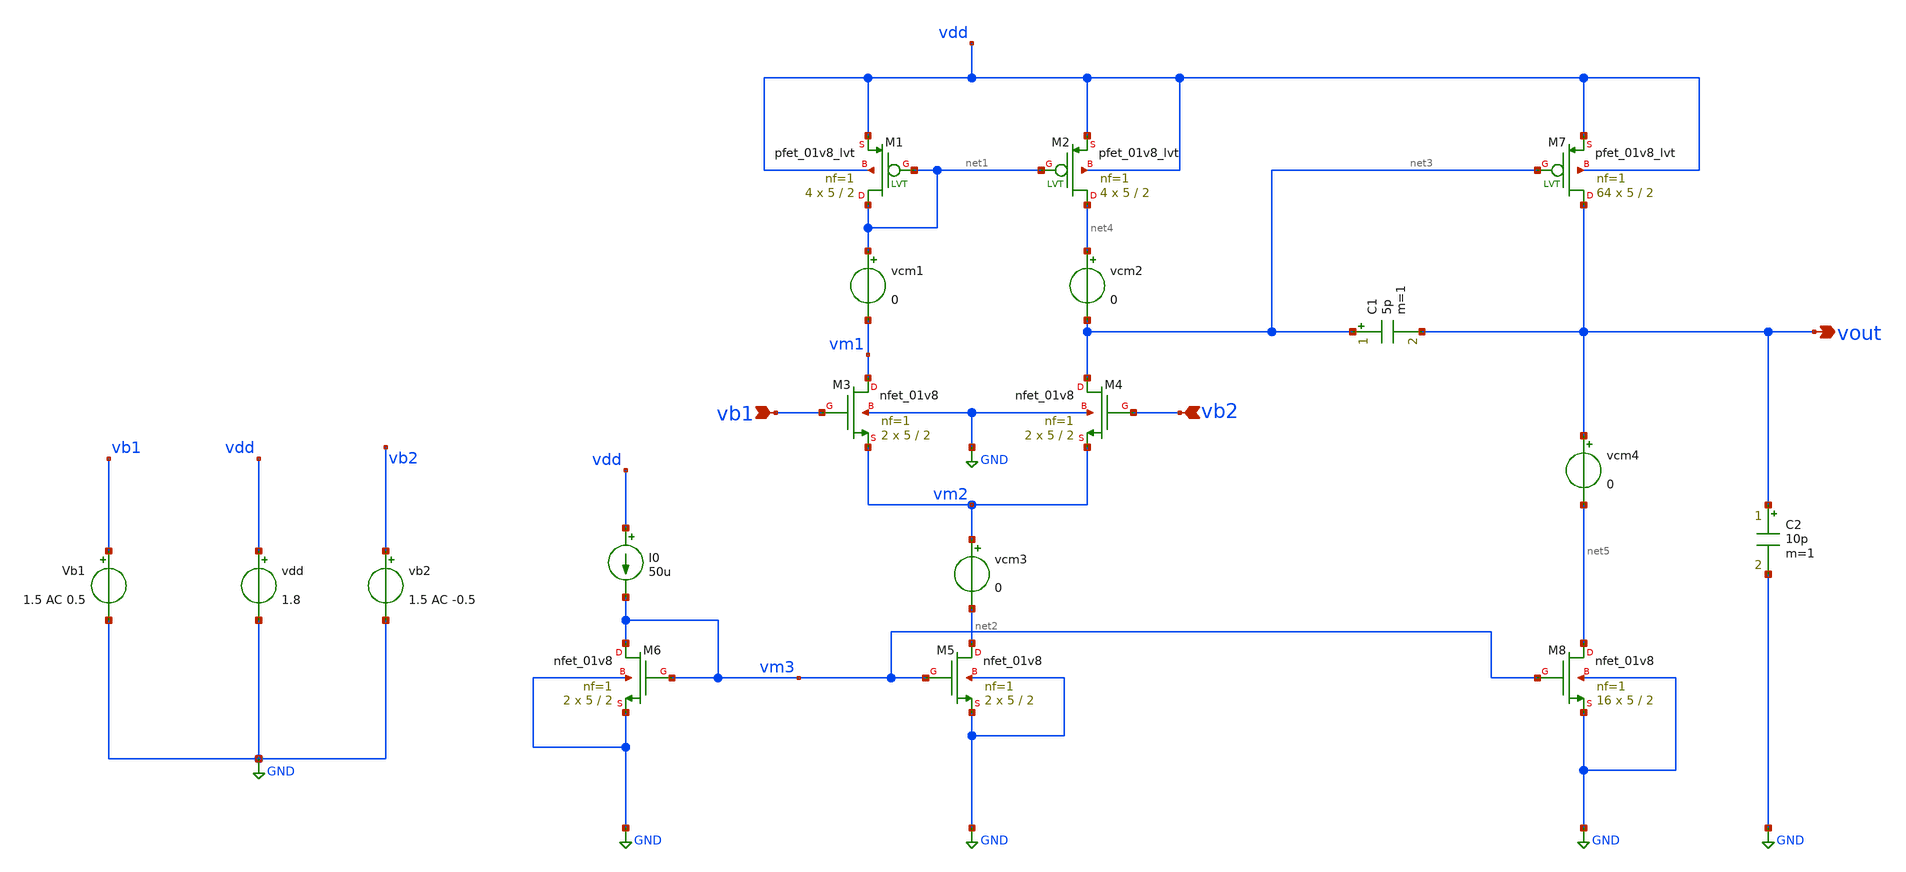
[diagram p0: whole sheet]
** sch_path: testbenches/Two_Stage_Differential_OpAmp_AC_Analysis.sch
**.subckt Two_Stage_Differential_OpAmp_AC_Analysis vb1 vout vb2
*.ipin vb1
*.opin vout
*.ipin vb2
XM5 net2 vm3 GND GND sky130_fd_pr__nfet_01v8 L=2 W=5 nf=1 ad='int((1 + 1)/2) * 5 / 1 * 0.29' as='int((1 + 2)/2) * 5 / 1 * 0.29'
+ pd='2*int((1 + 1)/2) * (5 / 1 + 0.29)' ps='2*int((1 + 2)/2) * (5 / 1 + 0.29)' nrd='0.29 / 5 ' nrs='0.29 / 5 '
+ sa=0 sb=0 sd=0 mult=2 m=2
I0 vdd vm3 50u
XM2 net4 net1 vdd vdd sky130_fd_pr__pfet_01v8_lvt L=2 W=5 nf=1 ad='int((1 + 1)/2) * 5 / 1 * 0.29' as='int((1 + 2)/2) * 5 / 1 * 0.29'
+ pd='2*int((1 + 1)/2) * (5 / 1 + 0.29)' ps='2*int((1 + 2)/2) * (5 / 1 + 0.29)' nrd='0.29 / 5 ' nrs='0.29 / 5 '
+ sa=0 sb=0 sd=0 mult=4 m=4
XM3 vm1 vb1 vm2 GND sky130_fd_pr__nfet_01v8 L=2 W=5 nf=1 ad='int((1 + 1)/2) * 5 / 1 * 0.29' as='int((1 + 2)/2) * 5 / 1 * 0.29'
+ pd='2*int((1 + 1)/2) * (5 / 1 + 0.29)' ps='2*int((1 + 2)/2) * (5 / 1 + 0.29)' nrd='0.29 / 5 ' nrs='0.29 / 5 '
+ sa=0 sb=0 sd=0 mult=2 m=2
XM4 net3 vb2 vm2 GND sky130_fd_pr__nfet_01v8 L=2 W=5 nf=1 ad='int((1 + 1)/2) * 5 / 1 * 0.29' as='int((1 + 2)/2) * 5 / 1 * 0.29'
+ pd='2*int((1 + 1)/2) * (5 / 1 + 0.29)' ps='2*int((1 + 2)/2) * (5 / 1 + 0.29)' nrd='0.29 / 5 ' nrs='0.29 / 5 '
+ sa=0 sb=0 sd=0 mult=2 m=2
XM6 vm3 vm3 GND GND sky130_fd_pr__nfet_01v8 L=2 W=5 nf=1 ad='int((1 + 1)/2) * 5 / 1 * 0.29' as='int((1 + 2)/2) * 5 / 1 * 0.29'
+ pd='2*int((1 + 1)/2) * (5 / 1 + 0.29)' ps='2*int((1 + 2)/2) * (5 / 1 + 0.29)' nrd='0.29 / 5 ' nrs='0.29 / 5 '
+ sa=0 sb=0 sd=0 mult=2 m=2
XM1 net1 net1 vdd vdd sky130_fd_pr__pfet_01v8_lvt L=2 W=5 nf=1 ad='int((1 + 1)/2) * 5 / 1 * 0.29' as='int((1 + 2)/2) * 5 / 1 * 0.29'
+ pd='2*int((1 + 1)/2) * (5 / 1 + 0.29)' ps='2*int((1 + 2)/2) * (5 / 1 + 0.29)' nrd='0.29 / 5 ' nrs='0.29 / 5 '
+ sa=0 sb=0 sd=0 mult=4 m=4
vcm3 vm2 net2 0
vcm1 net1 vm1 0
vcm2 net4 net3 0
XM7 vout net3 vdd vdd sky130_fd_pr__pfet_01v8_lvt L=2 W=5 nf=1 ad='int((1 + 1)/2) * 5 / 1 * 0.29' as='int((1 + 2)/2) * 5 / 1 * 0.29'
+ pd='2*int((1 + 1)/2) * (5 / 1 + 0.29)' ps='2*int((1 + 2)/2) * (5 / 1 + 0.29)' nrd='0.29 / 5 ' nrs='0.29 / 5 '
+ sa=0 sb=0 sd=0 mult=64 m=64
XM8 net5 vm3 GND GND sky130_fd_pr__nfet_01v8 L=2 W=5 nf=1 ad='int((1 + 1)/2) * 5 / 1 * 0.29' as='int((1 + 2)/2) * 5 / 1 * 0.29'
+ pd='2*int((1 + 1)/2) * (5 / 1 + 0.29)' ps='2*int((1 + 2)/2) * (5 / 1 + 0.29)' nrd='0.29 / 5 ' nrs='0.29 / 5 '
+ sa=0 sb=0 sd=0 mult=16 m=16
C1 net3 vout 5p m=1
vcm4 vout net5 0
C2 vout GND 10p m=1
vdd vdd GND 1.8
Vb1 vb1 GND 1.5 AC 0.5
vb2 vb2 GND 1.5 AC -0.5
**** begin user architecture code

** opencircuitdesign pdks install
.lib $::SKYWATER_MODELS/sky130.lib.spice tt




* ngspice commands
.temp 27

.ac dec 10 1 10G

.control
run
save all

set color0 = white

*Plotting gain and Phase
plot db(v(vout)) title 'Magnitude Response (Gain in dB)'
plot ph(v(vout))*(180/pi)

*Low-frequency gain (at first AC point)
let gain0 = db(v(vout))[0]

*3-DB bandwidth
meas ac BW_3DB when db(v(vout)) = (gain0-3)

*Unity Gain BW
meas ac UGB when db(v(vout)) = 0


.endc
.end



**** end user architecture code
**.ends
.GLOBAL GND
.end
